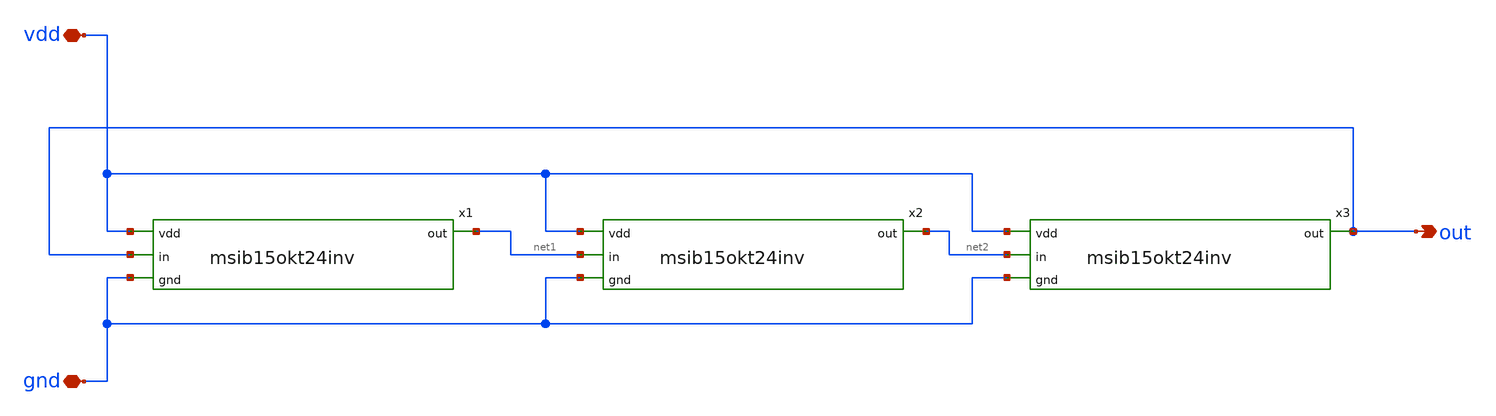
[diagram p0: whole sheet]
** sch_path: FILE SCH/ocilator3.sch
**.subckt ocilator3 vdd gnd out
*.iopin vdd
*.iopin gnd
*.opin out
x1 vdd out net1 gnd msib15okt24inv
x2 vdd net1 net2 gnd msib15okt24inv
x3 vdd net2 out gnd msib15okt24inv
**.ends
.end
